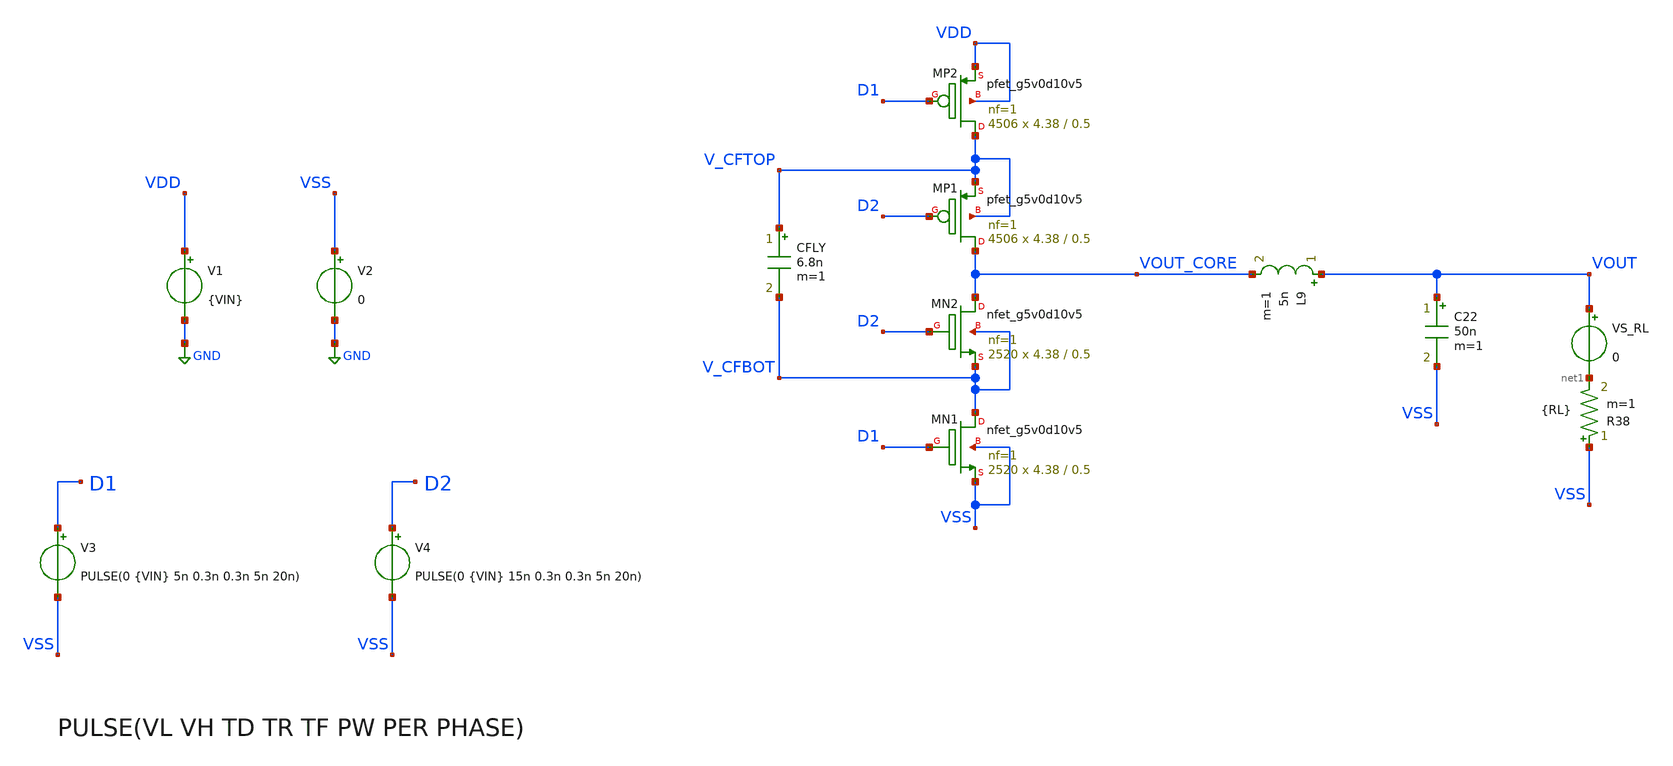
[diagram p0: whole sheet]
** sch_path: xschem/dev_switches/DCDC_v1p3_100MHz.sch
**.subckt DCDC_v1p3_100MHz
XMP1 VOUT_CORE D2 V_CFTOP V_CFTOP sky130_fd_pr__pfet_g5v0d10v5 L=0.5 W=4.38 nf=1 ad='int((nf+1)/2) * W/nf * 0.29'
+ as='int((nf+2)/2) * W/nf * 0.29' pd='2*int((nf+1)/2) * (W/nf + 0.29)' ps='2*int((nf+2)/2) * (W/nf + 0.29)'
+ nrd='0.29 / W' nrs='0.29 / W' sa=0 sb=0 sd=0 mult=4506 m=4506
XMN2 VOUT_CORE D2 V_CFBOT V_CFBOT sky130_fd_pr__nfet_g5v0d10v5 L=0.5 W=4.38 nf=1 ad='int((nf+1)/2) * W/nf * 0.29'
+ as='int((nf+2)/2) * W/nf * 0.29' pd='2*int((nf+1)/2) * (W/nf + 0.29)' ps='2*int((nf+2)/2) * (W/nf + 0.29)'
+ nrd='0.29 / W' nrs='0.29 / W' sa=0 sb=0 sd=0 mult=2520 m=2520
XMN1 V_CFBOT D1 VSS VSS sky130_fd_pr__nfet_g5v0d10v5 L=0.5 W=4.38 nf=1 ad='int((nf+1)/2) * W/nf * 0.29'
+ as='int((nf+2)/2) * W/nf * 0.29' pd='2*int((nf+1)/2) * (W/nf + 0.29)' ps='2*int((nf+2)/2) * (W/nf + 0.29)'
+ nrd='0.29 / W' nrs='0.29 / W' sa=0 sb=0 sd=0 mult=2520 m=2520
XMP2 V_CFTOP D1 VDD VDD sky130_fd_pr__pfet_g5v0d10v5 L=0.5 W=4.38 nf=1 ad='int((nf+1)/2) * W/nf * 0.29'
+ as='int((nf+2)/2) * W/nf * 0.29' pd='2*int((nf+1)/2) * (W/nf + 0.29)' ps='2*int((nf+2)/2) * (W/nf + 0.29)'
+ nrd='0.29 / W' nrs='0.29 / W' sa=0 sb=0 sd=0 mult=4506 m=4506
CFLY V_CFTOP V_CFBOT 6.8n m=1
V1 VDD GND {VIN}
V3 D1 VSS PULSE(0 {VIN} 5n 0.3n 0.3n 5n 20n)
V2 VSS GND 0
V4 D2 VSS PULSE(0 {VIN} 15n 0.3n 0.3n 5n 20n)
L9 VOUT VOUT_CORE 5n m=1
C22 VOUT VSS 50n m=1
R38 VSS net1 {RL} m=1
VS_RL VOUT net1 0
**** begin user architecture code


.param VIN = 20
.param RL = 50
*.option temp=70
.ic v(V_CFTOP) = VIN/2
.ic v(V_CFBOT) = 0
*.probe vd(MP2:G:S)

.param mc_mm_switch=0
*.lib /usr/share/pdk/sky130A/libs.tech/ngspice/sky130.lib.spice tt
.lib /home/jorge/Documents/Postdoc/share/pdk/sky130A/libs.tech/ngspice/sky130.lib.spice tt
*.include /usr/share/pdk/sky130A/libs.ref/sky130_fd_sc_hvl/spice/sky130_fd_sc_hvl.spice
.include /home/jorge/Documents/Postdoc/share/pdk/sky130A/libs.ref/sky130_fd_sc_hvl/spice/sky130_fd_sc_hvl.spice

.control
save all
tran 0.4n 2u
write DCDC_v1p3_100MHz.raw
.endc


**** end user architecture code
**.ends
.GLOBAL GND
.end
